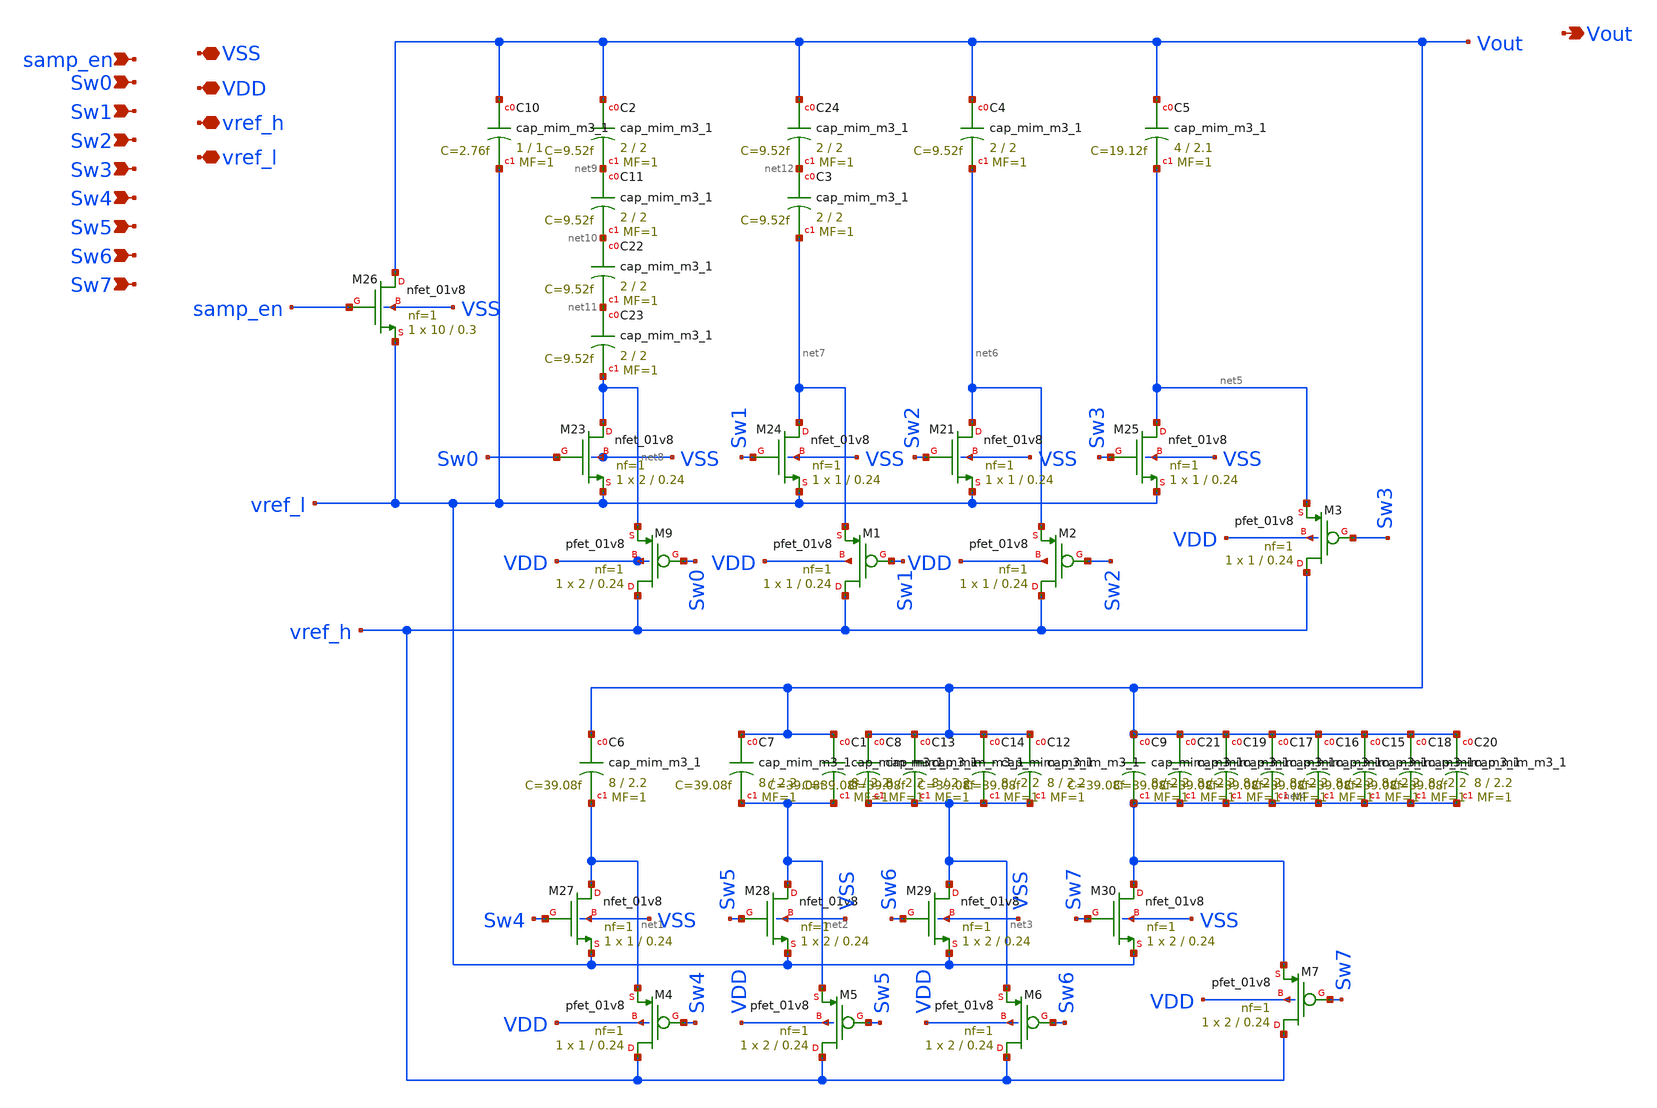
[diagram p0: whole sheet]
** sch_path: Tapeout/DAC/adc_8bit_DAC.sch
**.subckt adc_8bit_DAC Sw0 samp_en VSS VDD vref_l Vout Sw1 Sw2 Sw3 Sw4 Sw5 Sw6 Sw7 vref_h
*.ipin Sw0
*.ipin samp_en
*.iopin VSS
*.iopin VDD
*.iopin vref_l
*.opin Vout
*.ipin Sw1
*.ipin Sw2
*.ipin Sw3
*.ipin Sw4
*.ipin Sw5
*.ipin Sw6
*.ipin Sw7
*.iopin vref_h
XM23 net8 Sw0 vref_l VSS sky130_fd_pr__nfet_01v8 L=0.24 W=2 nf=1 ad='int((nf+1)/2) * W/nf * 0.29' as='int((nf+2)/2) * W/nf * 0.29'
+ pd='2*int((nf+1)/2) * (W/nf + 0.29)' ps='2*int((nf+2)/2) * (W/nf + 0.29)' nrd='0.29 / W' nrs='0.29 / W'
+ sa=0 sb=0 sd=0 mult=1 m=1
XM21 net6 Sw2 vref_l VSS sky130_fd_pr__nfet_01v8 L=0.24 W=1 nf=1 ad='int((nf+1)/2) * W/nf * 0.29' as='int((nf+2)/2) * W/nf * 0.29'
+ pd='2*int((nf+1)/2) * (W/nf + 0.29)' ps='2*int((nf+2)/2) * (W/nf + 0.29)' nrd='0.29 / W' nrs='0.29 / W'
+ sa=0 sb=0 sd=0 mult=1 m=1
XM24 net7 Sw1 vref_l VSS sky130_fd_pr__nfet_01v8 L=0.24 W=1 nf=1 ad='int((nf+1)/2) * W/nf * 0.29' as='int((nf+2)/2) * W/nf * 0.29'
+ pd='2*int((nf+1)/2) * (W/nf + 0.29)' ps='2*int((nf+2)/2) * (W/nf + 0.29)' nrd='0.29 / W' nrs='0.29 / W'
+ sa=0 sb=0 sd=0 mult=1 m=1
XM25 net5 Sw3 vref_l VSS sky130_fd_pr__nfet_01v8 L=0.24 W=1 nf=1 ad='int((nf+1)/2) * W/nf * 0.29' as='int((nf+2)/2) * W/nf * 0.29'
+ pd='2*int((nf+1)/2) * (W/nf + 0.29)' ps='2*int((nf+2)/2) * (W/nf + 0.29)' nrd='0.29 / W' nrs='0.29 / W'
+ sa=0 sb=0 sd=0 mult=1 m=1
XM26 Vout samp_en vref_l VSS sky130_fd_pr__nfet_01v8 L=0.3 W=10 nf=1 ad='int((nf+1)/2) * W/nf * 0.29'
+ as='int((nf+2)/2) * W/nf * 0.29' pd='2*int((nf+1)/2) * (W/nf + 0.29)' ps='2*int((nf+2)/2) * (W/nf + 0.29)'
+ nrd='0.29 / W' nrs='0.29 / W' sa=0 sb=0 sd=0 mult=1 m=1
XM27 net1 Sw4 vref_l VSS sky130_fd_pr__nfet_01v8 L=0.24 W=1 nf=1 ad='int((nf+1)/2) * W/nf * 0.29' as='int((nf+2)/2) * W/nf * 0.29'
+ pd='2*int((nf+1)/2) * (W/nf + 0.29)' ps='2*int((nf+2)/2) * (W/nf + 0.29)' nrd='0.29 / W' nrs='0.29 / W'
+ sa=0 sb=0 sd=0 mult=1 m=1
XM28 net2 Sw5 vref_l VSS sky130_fd_pr__nfet_01v8 L=0.24 W=2 nf=1 ad='int((nf+1)/2) * W/nf * 0.29' as='int((nf+2)/2) * W/nf * 0.29'
+ pd='2*int((nf+1)/2) * (W/nf + 0.29)' ps='2*int((nf+2)/2) * (W/nf + 0.29)' nrd='0.29 / W' nrs='0.29 / W'
+ sa=0 sb=0 sd=0 mult=1 m=1
XM29 net3 Sw6 vref_l VSS sky130_fd_pr__nfet_01v8 L=0.24 W=2 nf=1 ad='int((nf+1)/2) * W/nf * 0.29' as='int((nf+2)/2) * W/nf * 0.29'
+ pd='2*int((nf+1)/2) * (W/nf + 0.29)' ps='2*int((nf+2)/2) * (W/nf + 0.29)' nrd='0.29 / W' nrs='0.29 / W'
+ sa=0 sb=0 sd=0 mult=1 m=1
XM30 net4 Sw7 vref_l VSS sky130_fd_pr__nfet_01v8 L=0.24 W=2 nf=1 ad='int((nf+1)/2) * W/nf * 0.29' as='int((nf+2)/2) * W/nf * 0.29'
+ pd='2*int((nf+1)/2) * (W/nf + 0.29)' ps='2*int((nf+2)/2) * (W/nf + 0.29)' nrd='0.29 / W' nrs='0.29 / W'
+ sa=0 sb=0 sd=0 mult=1 m=1
XM9 vref_h Sw0 net8 VDD sky130_fd_pr__pfet_01v8 L=0.24 W=2 nf=1 ad='int((nf+1)/2) * W/nf * 0.29' as='int((nf+2)/2) * W/nf * 0.29'
+ pd='2*int((nf+1)/2) * (W/nf + 0.29)' ps='2*int((nf+2)/2) * (W/nf + 0.29)' nrd='0.29 / W' nrs='0.29 / W'
+ sa=0 sb=0 sd=0 mult=1 m=1
XM1 vref_h Sw1 net7 VDD sky130_fd_pr__pfet_01v8 L=0.24 W=1 nf=1 ad='int((nf+1)/2) * W/nf * 0.29' as='int((nf+2)/2) * W/nf * 0.29'
+ pd='2*int((nf+1)/2) * (W/nf + 0.29)' ps='2*int((nf+2)/2) * (W/nf + 0.29)' nrd='0.29 / W' nrs='0.29 / W'
+ sa=0 sb=0 sd=0 mult=1 m=1
XM2 vref_h Sw2 net6 VDD sky130_fd_pr__pfet_01v8 L=0.24 W=1 nf=1 ad='int((nf+1)/2) * W/nf * 0.29' as='int((nf+2)/2) * W/nf * 0.29'
+ pd='2*int((nf+1)/2) * (W/nf + 0.29)' ps='2*int((nf+2)/2) * (W/nf + 0.29)' nrd='0.29 / W' nrs='0.29 / W'
+ sa=0 sb=0 sd=0 mult=1 m=1
XM3 vref_h Sw3 net5 VDD sky130_fd_pr__pfet_01v8 L=0.24 W=1 nf=1 ad='int((nf+1)/2) * W/nf * 0.29' as='int((nf+2)/2) * W/nf * 0.29'
+ pd='2*int((nf+1)/2) * (W/nf + 0.29)' ps='2*int((nf+2)/2) * (W/nf + 0.29)' nrd='0.29 / W' nrs='0.29 / W'
+ sa=0 sb=0 sd=0 mult=1 m=1
XM4 vref_h Sw4 net1 VDD sky130_fd_pr__pfet_01v8 L=0.24 W=1 nf=1 ad='int((nf+1)/2) * W/nf * 0.29' as='int((nf+2)/2) * W/nf * 0.29'
+ pd='2*int((nf+1)/2) * (W/nf + 0.29)' ps='2*int((nf+2)/2) * (W/nf + 0.29)' nrd='0.29 / W' nrs='0.29 / W'
+ sa=0 sb=0 sd=0 mult=1 m=1
XM5 vref_h Sw5 net2 VDD sky130_fd_pr__pfet_01v8 L=0.24 W=2 nf=1 ad='int((nf+1)/2) * W/nf * 0.29' as='int((nf+2)/2) * W/nf * 0.29'
+ pd='2*int((nf+1)/2) * (W/nf + 0.29)' ps='2*int((nf+2)/2) * (W/nf + 0.29)' nrd='0.29 / W' nrs='0.29 / W'
+ sa=0 sb=0 sd=0 mult=1 m=1
XM6 vref_h Sw6 net3 VDD sky130_fd_pr__pfet_01v8 L=0.24 W=2 nf=1 ad='int((nf+1)/2) * W/nf * 0.29' as='int((nf+2)/2) * W/nf * 0.29'
+ pd='2*int((nf+1)/2) * (W/nf + 0.29)' ps='2*int((nf+2)/2) * (W/nf + 0.29)' nrd='0.29 / W' nrs='0.29 / W'
+ sa=0 sb=0 sd=0 mult=1 m=1
XM7 vref_h Sw7 net4 VDD sky130_fd_pr__pfet_01v8 L=0.24 W=2 nf=1 ad='int((nf+1)/2) * W/nf * 0.29' as='int((nf+2)/2) * W/nf * 0.29'
+ pd='2*int((nf+1)/2) * (W/nf + 0.29)' ps='2*int((nf+2)/2) * (W/nf + 0.29)' nrd='0.29 / W' nrs='0.29 / W'
+ sa=0 sb=0 sd=0 mult=1 m=1
XC6 Vout net1 sky130_fd_pr__cap_mim_m3_1 W=8 L=2.2 MF=1 m=1
XC2 Vout net9 sky130_fd_pr__cap_mim_m3_1 W=2 L=2 MF=1 m=1
XC10 Vout vref_l sky130_fd_pr__cap_mim_m3_1 W=1 L=1 MF=1 m=1
XC11 net9 net10 sky130_fd_pr__cap_mim_m3_1 W=2 L=2 MF=1 m=1
XC22 net10 net11 sky130_fd_pr__cap_mim_m3_1 W=2 L=2 MF=1 m=1
XC23 net11 net8 sky130_fd_pr__cap_mim_m3_1 W=2 L=2 MF=1 m=1
XC24 Vout net12 sky130_fd_pr__cap_mim_m3_1 W=2 L=2 MF=1 m=1
XC3 net12 net7 sky130_fd_pr__cap_mim_m3_1 W=2 L=2 MF=1 m=1
XC4 Vout net6 sky130_fd_pr__cap_mim_m3_1 W=2 L=2 MF=1 m=1
XC5 Vout net5 sky130_fd_pr__cap_mim_m3_1 W=4 L=2.1 MF=1 m=1
XC7 Vout net2 sky130_fd_pr__cap_mim_m3_1 W=8 L=2.2 MF=1 m=1
XC1 Vout net2 sky130_fd_pr__cap_mim_m3_1 W=8 L=2.2 MF=1 m=1
XC8 Vout net3 sky130_fd_pr__cap_mim_m3_1 W=8 L=2.2 MF=1 m=1
XC13 Vout net3 sky130_fd_pr__cap_mim_m3_1 W=8 L=2.2 MF=1 m=1
XC14 Vout net3 sky130_fd_pr__cap_mim_m3_1 W=8 L=2.2 MF=1 m=1
XC12 Vout net3 sky130_fd_pr__cap_mim_m3_1 W=8 L=2.2 MF=1 m=1
XC9 Vout net4 sky130_fd_pr__cap_mim_m3_1 W=8 L=2.2 MF=1 m=1
XC21 Vout net4 sky130_fd_pr__cap_mim_m3_1 W=8 L=2.2 MF=1 m=1
XC19 Vout net4 sky130_fd_pr__cap_mim_m3_1 W=8 L=2.2 MF=1 m=1
XC17 Vout net4 sky130_fd_pr__cap_mim_m3_1 W=8 L=2.2 MF=1 m=1
XC16 Vout net4 sky130_fd_pr__cap_mim_m3_1 W=8 L=2.2 MF=1 m=1
XC15 Vout net4 sky130_fd_pr__cap_mim_m3_1 W=8 L=2.2 MF=1 m=1
XC18 Vout net4 sky130_fd_pr__cap_mim_m3_1 W=8 L=2.2 MF=1 m=1
XC20 Vout net4 sky130_fd_pr__cap_mim_m3_1 W=8 L=2.2 MF=1 m=1
**.ends
.end
